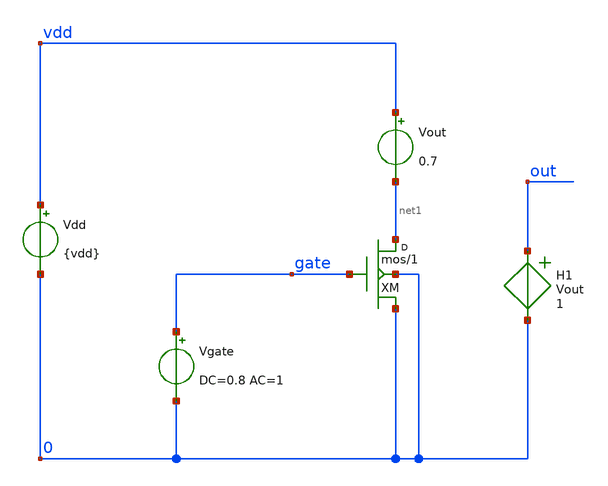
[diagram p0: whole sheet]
** sch_path: design/bandgap_cascurr_cell_sw/test/tb_bandgap_cascurr_cell_sw.sch
**.subckt tb_bandgap_cascurr_cell_sw
Vdd vdd 0 {vdd}
Vgate gate 0 DC=0.8 AC=1
H1 out 0 Vout 1
Vout vdd net1 0.7
XXM net1 gate 0 0 mos m=1
**** begin user architecture code


.param temp=27
.temp 27

.lib sky130_fd_pr/models/sky130.lib.spice tt

.param vdd=1.8
.param bias=1u

.options savecurrents

.save all @m.xmcurr.msky130_fd_pr__pfet_01v8_lvt[vdsat] @m.xmcurr.msky130_fd_pr__pfet_01v8_lvt[vth] @m.xmcurr.msky130_fd_pr__pfet_01v8_lvt[gm]

.dc vgate 0.5 0.9 0.01
.noise v(out) Vgate dec 10 1 100Meg


**** end user architecture code
**.ends
.end
